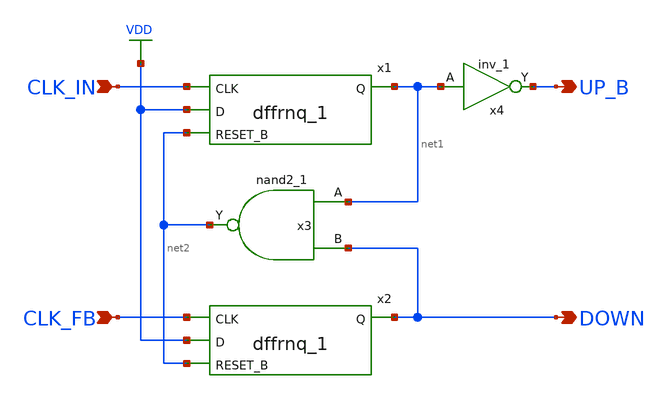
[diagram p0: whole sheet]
** sch_path: designs/libs/core_analog/pfd/pfd.sch
**.subckt pfd UP_B DOWN CLK_IN CLK_FB
*.opin UP_B
*.opin DOWN
*.ipin CLK_IN
*.ipin CLK_FB
x1 VDD net2 CLK_IN net1 VDD VDD GND GND gf180mcu_fd_sc_mcu7t5v0__dffrnq_1
x2 VDD net2 CLK_FB DOWN VDD VDD GND GND gf180mcu_fd_sc_mcu7t5v0__dffrnq_1
x3 net1 DOWN net2 VDD VDD GND GND gf180mcu_fd_sc_mcu7t5v0__nand2_1
x4 net1 UP_B VDD VDD GND GND gf180mcu_fd_sc_mcu7t5v0__inv_1
**.ends
.GLOBAL VDD
.end
